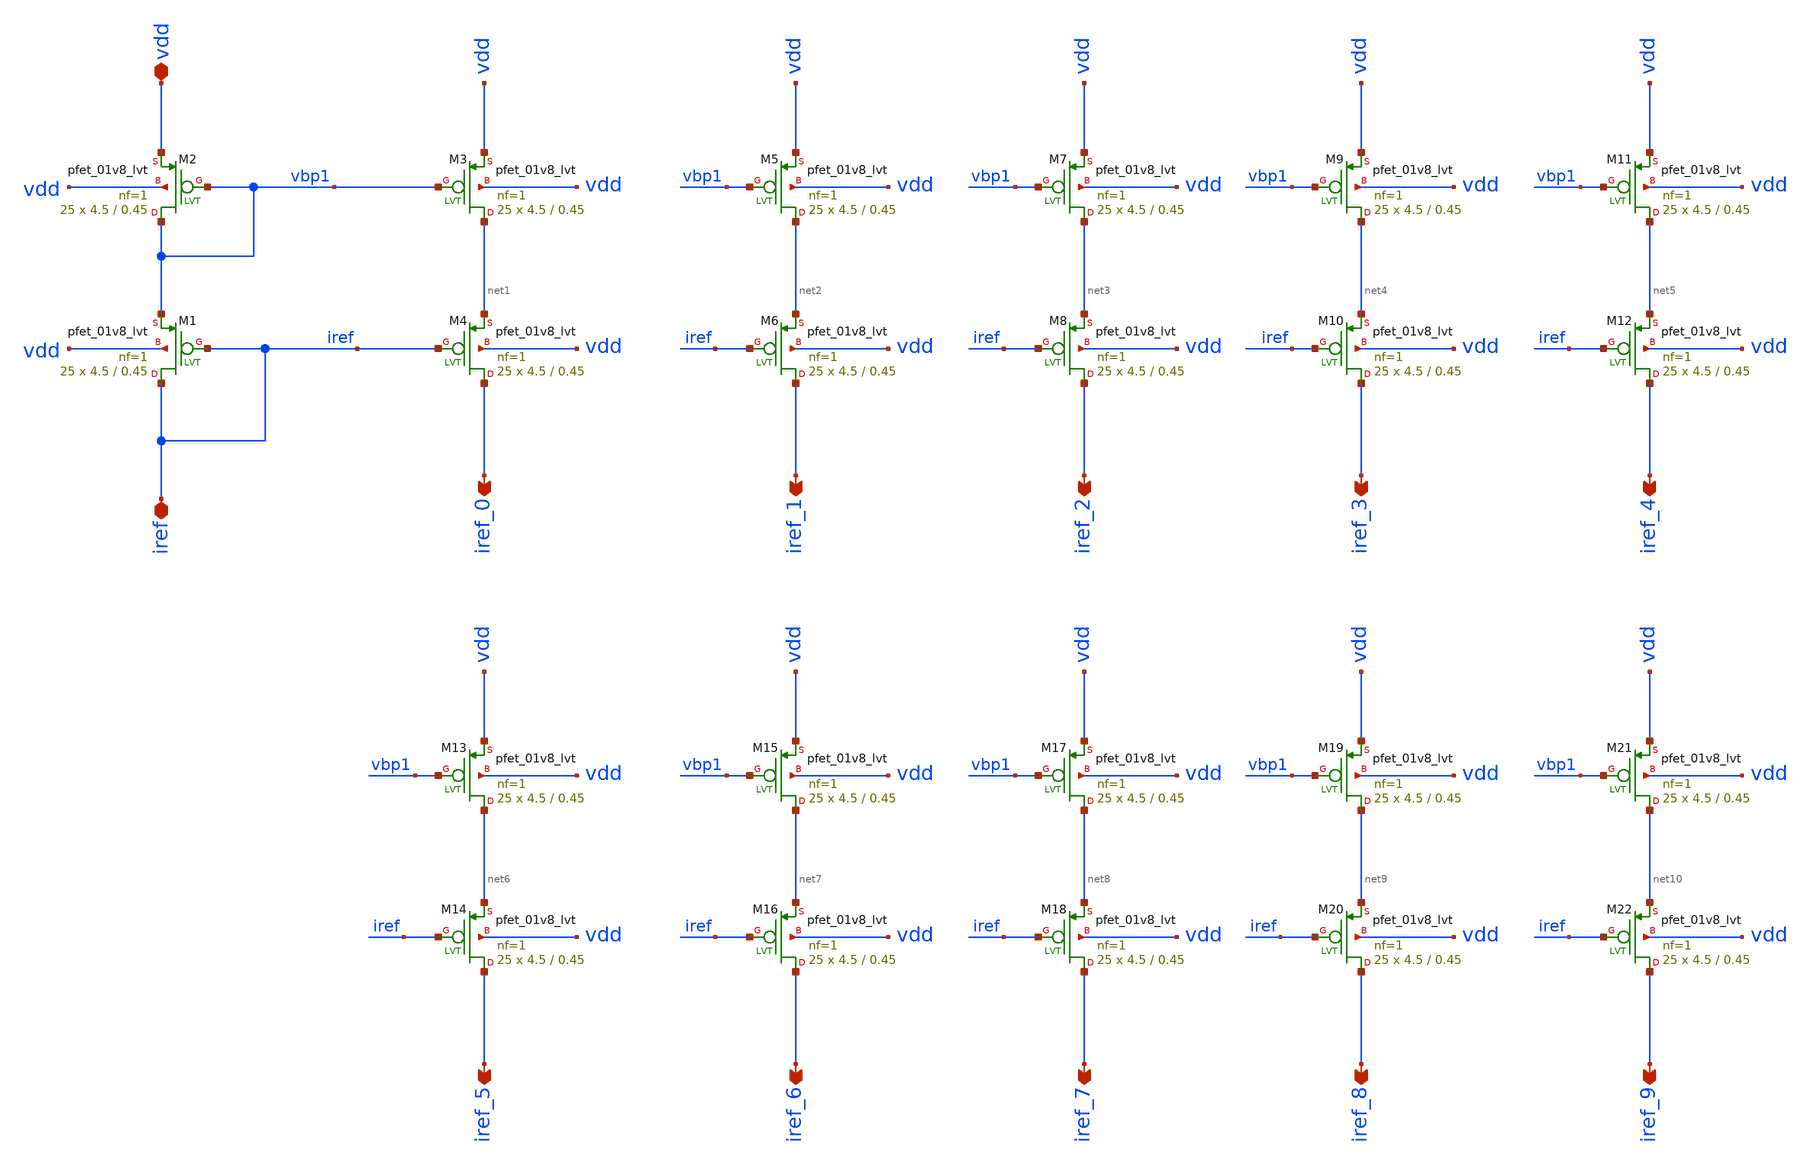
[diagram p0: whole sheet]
** sch_path: xschem/bias.sch
**.subckt bias iref vdd iref_0 iref_1 iref_2 iref_3 iref_4 iref_5 iref_6 iref_7 iref_8 iref_9
*.iopin iref
*.iopin vdd
*.opin iref_0
*.opin iref_1
*.opin iref_2
*.opin iref_3
*.opin iref_4
*.opin iref_5
*.opin iref_6
*.opin iref_7
*.opin iref_8
*.opin iref_9
XM1 iref iref vbp1 vdd sky130_fd_pr__pfet_01v8_lvt L=0.45 W=4.5 nf=1 ad='int((nf+1)/2) * W/nf * 0.29'
+ as='int((nf+2)/2) * W/nf * 0.29' pd='2*int((nf+1)/2) * (W/nf + 0.29)' ps='2*int((nf+2)/2) * (W/nf + 0.29)'
+ nrd='0.29 / W' nrs='0.29 / W' sa=0 sb=0 sd=0 mult=25 m=25
XM2 vbp1 vbp1 vdd vdd sky130_fd_pr__pfet_01v8_lvt L=0.45 W=4.5 nf=1 ad='int((nf+1)/2) * W/nf * 0.29'
+ as='int((nf+2)/2) * W/nf * 0.29' pd='2*int((nf+1)/2) * (W/nf + 0.29)' ps='2*int((nf+2)/2) * (W/nf + 0.29)'
+ nrd='0.29 / W' nrs='0.29 / W' sa=0 sb=0 sd=0 mult=25 m=25
XM3 net1 vbp1 vdd vdd sky130_fd_pr__pfet_01v8_lvt L=0.45 W=4.5 nf=1 ad='int((nf+1)/2) * W/nf * 0.29'
+ as='int((nf+2)/2) * W/nf * 0.29' pd='2*int((nf+1)/2) * (W/nf + 0.29)' ps='2*int((nf+2)/2) * (W/nf + 0.29)'
+ nrd='0.29 / W' nrs='0.29 / W' sa=0 sb=0 sd=0 mult=25 m=25
XM4 iref_0 iref net1 vdd sky130_fd_pr__pfet_01v8_lvt L=0.45 W=4.5 nf=1 ad='int((nf+1)/2) * W/nf * 0.29'
+ as='int((nf+2)/2) * W/nf * 0.29' pd='2*int((nf+1)/2) * (W/nf + 0.29)' ps='2*int((nf+2)/2) * (W/nf + 0.29)'
+ nrd='0.29 / W' nrs='0.29 / W' sa=0 sb=0 sd=0 mult=25 m=25
XM5 net2 vbp1 vdd vdd sky130_fd_pr__pfet_01v8_lvt L=0.45 W=4.5 nf=1 ad='int((nf+1)/2) * W/nf * 0.29'
+ as='int((nf+2)/2) * W/nf * 0.29' pd='2*int((nf+1)/2) * (W/nf + 0.29)' ps='2*int((nf+2)/2) * (W/nf + 0.29)'
+ nrd='0.29 / W' nrs='0.29 / W' sa=0 sb=0 sd=0 mult=25 m=25
XM6 iref_1 iref net2 vdd sky130_fd_pr__pfet_01v8_lvt L=0.45 W=4.5 nf=1 ad='int((nf+1)/2) * W/nf * 0.29'
+ as='int((nf+2)/2) * W/nf * 0.29' pd='2*int((nf+1)/2) * (W/nf + 0.29)' ps='2*int((nf+2)/2) * (W/nf + 0.29)'
+ nrd='0.29 / W' nrs='0.29 / W' sa=0 sb=0 sd=0 mult=25 m=25
XM7 net3 vbp1 vdd vdd sky130_fd_pr__pfet_01v8_lvt L=0.45 W=4.5 nf=1 ad='int((nf+1)/2) * W/nf * 0.29'
+ as='int((nf+2)/2) * W/nf * 0.29' pd='2*int((nf+1)/2) * (W/nf + 0.29)' ps='2*int((nf+2)/2) * (W/nf + 0.29)'
+ nrd='0.29 / W' nrs='0.29 / W' sa=0 sb=0 sd=0 mult=25 m=25
XM8 iref_2 iref net3 vdd sky130_fd_pr__pfet_01v8_lvt L=0.45 W=4.5 nf=1 ad='int((nf+1)/2) * W/nf * 0.29'
+ as='int((nf+2)/2) * W/nf * 0.29' pd='2*int((nf+1)/2) * (W/nf + 0.29)' ps='2*int((nf+2)/2) * (W/nf + 0.29)'
+ nrd='0.29 / W' nrs='0.29 / W' sa=0 sb=0 sd=0 mult=25 m=25
XM9 net4 vbp1 vdd vdd sky130_fd_pr__pfet_01v8_lvt L=0.45 W=4.5 nf=1 ad='int((nf+1)/2) * W/nf * 0.29'
+ as='int((nf+2)/2) * W/nf * 0.29' pd='2*int((nf+1)/2) * (W/nf + 0.29)' ps='2*int((nf+2)/2) * (W/nf + 0.29)'
+ nrd='0.29 / W' nrs='0.29 / W' sa=0 sb=0 sd=0 mult=25 m=25
XM10 iref_3 iref net4 vdd sky130_fd_pr__pfet_01v8_lvt L=0.45 W=4.5 nf=1 ad='int((nf+1)/2) * W/nf * 0.29'
+ as='int((nf+2)/2) * W/nf * 0.29' pd='2*int((nf+1)/2) * (W/nf + 0.29)' ps='2*int((nf+2)/2) * (W/nf + 0.29)'
+ nrd='0.29 / W' nrs='0.29 / W' sa=0 sb=0 sd=0 mult=25 m=25
XM11 net5 vbp1 vdd vdd sky130_fd_pr__pfet_01v8_lvt L=0.45 W=4.5 nf=1 ad='int((nf+1)/2) * W/nf * 0.29'
+ as='int((nf+2)/2) * W/nf * 0.29' pd='2*int((nf+1)/2) * (W/nf + 0.29)' ps='2*int((nf+2)/2) * (W/nf + 0.29)'
+ nrd='0.29 / W' nrs='0.29 / W' sa=0 sb=0 sd=0 mult=25 m=25
XM12 iref_4 iref net5 vdd sky130_fd_pr__pfet_01v8_lvt L=0.45 W=4.5 nf=1 ad='int((nf+1)/2) * W/nf * 0.29'
+ as='int((nf+2)/2) * W/nf * 0.29' pd='2*int((nf+1)/2) * (W/nf + 0.29)' ps='2*int((nf+2)/2) * (W/nf + 0.29)'
+ nrd='0.29 / W' nrs='0.29 / W' sa=0 sb=0 sd=0 mult=25 m=25
XM13 net6 vbp1 vdd vdd sky130_fd_pr__pfet_01v8_lvt L=0.45 W=4.5 nf=1 ad='int((nf+1)/2) * W/nf * 0.29'
+ as='int((nf+2)/2) * W/nf * 0.29' pd='2*int((nf+1)/2) * (W/nf + 0.29)' ps='2*int((nf+2)/2) * (W/nf + 0.29)'
+ nrd='0.29 / W' nrs='0.29 / W' sa=0 sb=0 sd=0 mult=25 m=25
XM14 iref_5 iref net6 vdd sky130_fd_pr__pfet_01v8_lvt L=0.45 W=4.5 nf=1 ad='int((nf+1)/2) * W/nf * 0.29'
+ as='int((nf+2)/2) * W/nf * 0.29' pd='2*int((nf+1)/2) * (W/nf + 0.29)' ps='2*int((nf+2)/2) * (W/nf + 0.29)'
+ nrd='0.29 / W' nrs='0.29 / W' sa=0 sb=0 sd=0 mult=25 m=25
XM15 net7 vbp1 vdd vdd sky130_fd_pr__pfet_01v8_lvt L=0.45 W=4.5 nf=1 ad='int((nf+1)/2) * W/nf * 0.29'
+ as='int((nf+2)/2) * W/nf * 0.29' pd='2*int((nf+1)/2) * (W/nf + 0.29)' ps='2*int((nf+2)/2) * (W/nf + 0.29)'
+ nrd='0.29 / W' nrs='0.29 / W' sa=0 sb=0 sd=0 mult=25 m=25
XM16 iref_6 iref net7 vdd sky130_fd_pr__pfet_01v8_lvt L=0.45 W=4.5 nf=1 ad='int((nf+1)/2) * W/nf * 0.29'
+ as='int((nf+2)/2) * W/nf * 0.29' pd='2*int((nf+1)/2) * (W/nf + 0.29)' ps='2*int((nf+2)/2) * (W/nf + 0.29)'
+ nrd='0.29 / W' nrs='0.29 / W' sa=0 sb=0 sd=0 mult=25 m=25
XM17 net8 vbp1 vdd vdd sky130_fd_pr__pfet_01v8_lvt L=0.45 W=4.5 nf=1 ad='int((nf+1)/2) * W/nf * 0.29'
+ as='int((nf+2)/2) * W/nf * 0.29' pd='2*int((nf+1)/2) * (W/nf + 0.29)' ps='2*int((nf+2)/2) * (W/nf + 0.29)'
+ nrd='0.29 / W' nrs='0.29 / W' sa=0 sb=0 sd=0 mult=25 m=25
XM18 iref_7 iref net8 vdd sky130_fd_pr__pfet_01v8_lvt L=0.45 W=4.5 nf=1 ad='int((nf+1)/2) * W/nf * 0.29'
+ as='int((nf+2)/2) * W/nf * 0.29' pd='2*int((nf+1)/2) * (W/nf + 0.29)' ps='2*int((nf+2)/2) * (W/nf + 0.29)'
+ nrd='0.29 / W' nrs='0.29 / W' sa=0 sb=0 sd=0 mult=25 m=25
XM19 net9 vbp1 vdd vdd sky130_fd_pr__pfet_01v8_lvt L=0.45 W=4.5 nf=1 ad='int((nf+1)/2) * W/nf * 0.29'
+ as='int((nf+2)/2) * W/nf * 0.29' pd='2*int((nf+1)/2) * (W/nf + 0.29)' ps='2*int((nf+2)/2) * (W/nf + 0.29)'
+ nrd='0.29 / W' nrs='0.29 / W' sa=0 sb=0 sd=0 mult=25 m=25
XM20 iref_8 iref net9 vdd sky130_fd_pr__pfet_01v8_lvt L=0.45 W=4.5 nf=1 ad='int((nf+1)/2) * W/nf * 0.29'
+ as='int((nf+2)/2) * W/nf * 0.29' pd='2*int((nf+1)/2) * (W/nf + 0.29)' ps='2*int((nf+2)/2) * (W/nf + 0.29)'
+ nrd='0.29 / W' nrs='0.29 / W' sa=0 sb=0 sd=0 mult=25 m=25
XM21 net10 vbp1 vdd vdd sky130_fd_pr__pfet_01v8_lvt L=0.45 W=4.5 nf=1 ad='int((nf+1)/2) * W/nf * 0.29'
+ as='int((nf+2)/2) * W/nf * 0.29' pd='2*int((nf+1)/2) * (W/nf + 0.29)' ps='2*int((nf+2)/2) * (W/nf + 0.29)'
+ nrd='0.29 / W' nrs='0.29 / W' sa=0 sb=0 sd=0 mult=25 m=25
XM22 iref_9 iref net10 vdd sky130_fd_pr__pfet_01v8_lvt L=0.45 W=4.5 nf=1 ad='int((nf+1)/2) * W/nf * 0.29'
+ as='int((nf+2)/2) * W/nf * 0.29' pd='2*int((nf+1)/2) * (W/nf + 0.29)' ps='2*int((nf+2)/2) * (W/nf + 0.29)'
+ nrd='0.29 / W' nrs='0.29 / W' sa=0 sb=0 sd=0 mult=25 m=25
**.ends
.end
